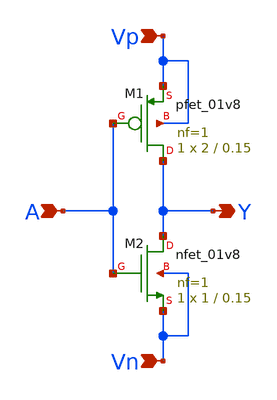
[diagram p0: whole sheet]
** sch_path: Inverter/Schematic/inv.sch
**.subckt inv A Y Vp Vn
*.ipin A
*.opin Y
*.ipin Vp
*.ipin Vn
XM1 Y A Vp Vp sky130_fd_pr__pfet_01v8 L=0.15 W=2 nf=1 ad='int((nf+1)/2) * W/nf * 0.29' as='int((nf+2)/2) * W/nf * 0.29'
+ pd='2*int((nf+1)/2) * (W/nf + 0.29)' ps='2*int((nf+2)/2) * (W/nf + 0.29)' nrd='0.29 / W' nrs='0.29 / W'
+ sa=0 sb=0 sd=0 mult=1 m=1
XM2 Y A Vn Vn sky130_fd_pr__nfet_01v8 L=0.15 W=1 nf=1 ad='int((nf+1)/2) * W/nf * 0.29' as='int((nf+2)/2) * W/nf * 0.29'
+ pd='2*int((nf+1)/2) * (W/nf + 0.29)' ps='2*int((nf+2)/2) * (W/nf + 0.29)' nrd='0.29 / W' nrs='0.29 / W'
+ sa=0 sb=0 sd=0 mult=1 m=1
**.ends
.end
